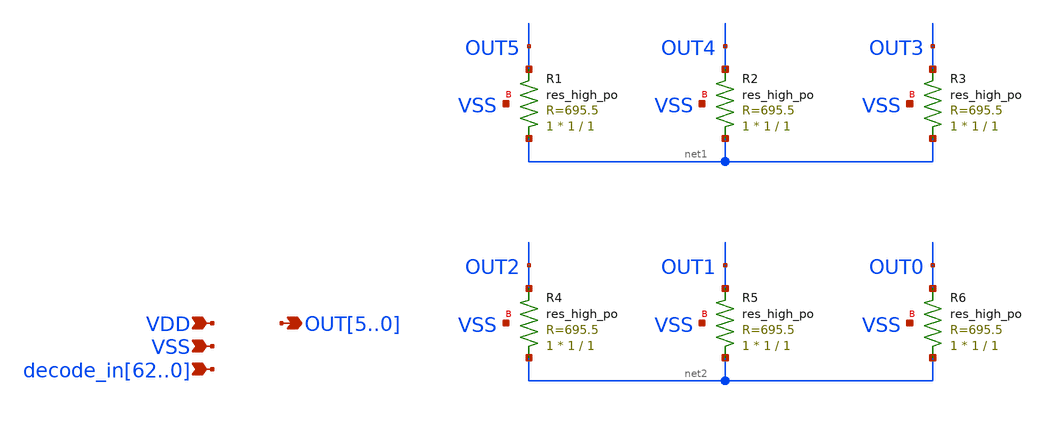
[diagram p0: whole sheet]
** sch_path: schematics/decoder_top.sch
**.subckt decoder_top
*+ decode_in62,decode_in61,decode_in60,decode_in59,decode_in58,decode_in57,decode_in56,decode_in55,decode_in54,decode_in53,decode_in52,decode_in51,decode_in50,decode_in49,decode_in48,decode_in47,decode_in46,decode_in45,decode_in44,decode_in43,decode_in42,decode_in41,decode_in40,decode_in39,decode_in38,decode_in37,decode_in36,decode_in35,decode_in34,decode_in33,decode_in32,decode_in31,decode_in30,decode_in29,decode_in28,decode_in27,decode_in26,decode_in25,decode_in24,decode_in23,decode_in22,decode_in21,decode_in20,decode_in19,decode_in18,decode_in17,decode_in16,decode_in15,decode_in14,decode_in13,decode_in12,decode_in11,decode_in10,decode_in9,decode_in8,decode_in7,decode_in6,decode_in5,decode_in4,decode_in3,decode_in2,decode_in1,decode_in0 VDD VSS OUT5,OUT4,OUT3,OUT2,OUT1,OUT0
*.ipin
*+ decode_in62,decode_in61,decode_in60,decode_in59,decode_in58,decode_in57,decode_in56,decode_in55,decode_in54,decode_in53,decode_in52,decode_in51,decode_in50,decode_in49,decode_in48,decode_in47,decode_in46,decode_in45,decode_in44,decode_in43,decode_in42,decode_in41,decode_in40,decode_in39,decode_in38,decode_in37,decode_in36,decode_in35,decode_in34,decode_in33,decode_in32,decode_in31,decode_in30,decode_in29,decode_in28,decode_in27,decode_in26,decode_in25,decode_in24,decode_in23,decode_in22,decode_in21,decode_in20,decode_in19,decode_in18,decode_in17,decode_in16,decode_in15,decode_in14,decode_in13,decode_in12,decode_in11,decode_in10,decode_in9,decode_in8,decode_in7,decode_in6,decode_in5,decode_in4,decode_in3,decode_in2,decode_in1,decode_in0
*.ipin VDD
*.ipin VSS
*.opin OUT5,OUT4,OUT3,OUT2,OUT1,OUT0
XR1 net1 OUT5 VSS sky130_fd_pr__res_high_po W=1 L=1 mult=1 m=1
XR2 net1 OUT4 VSS sky130_fd_pr__res_high_po W=1 L=1 mult=1 m=1
XR3 net1 OUT3 VSS sky130_fd_pr__res_high_po W=1 L=1 mult=1 m=1
XR4 net2 OUT2 VSS sky130_fd_pr__res_high_po W=1 L=1 mult=1 m=1
XR5 net2 OUT1 VSS sky130_fd_pr__res_high_po W=1 L=1 mult=1 m=1
XR6 net2 OUT0 VSS sky130_fd_pr__res_high_po W=1 L=1 mult=1 m=1
**.ends
.end
